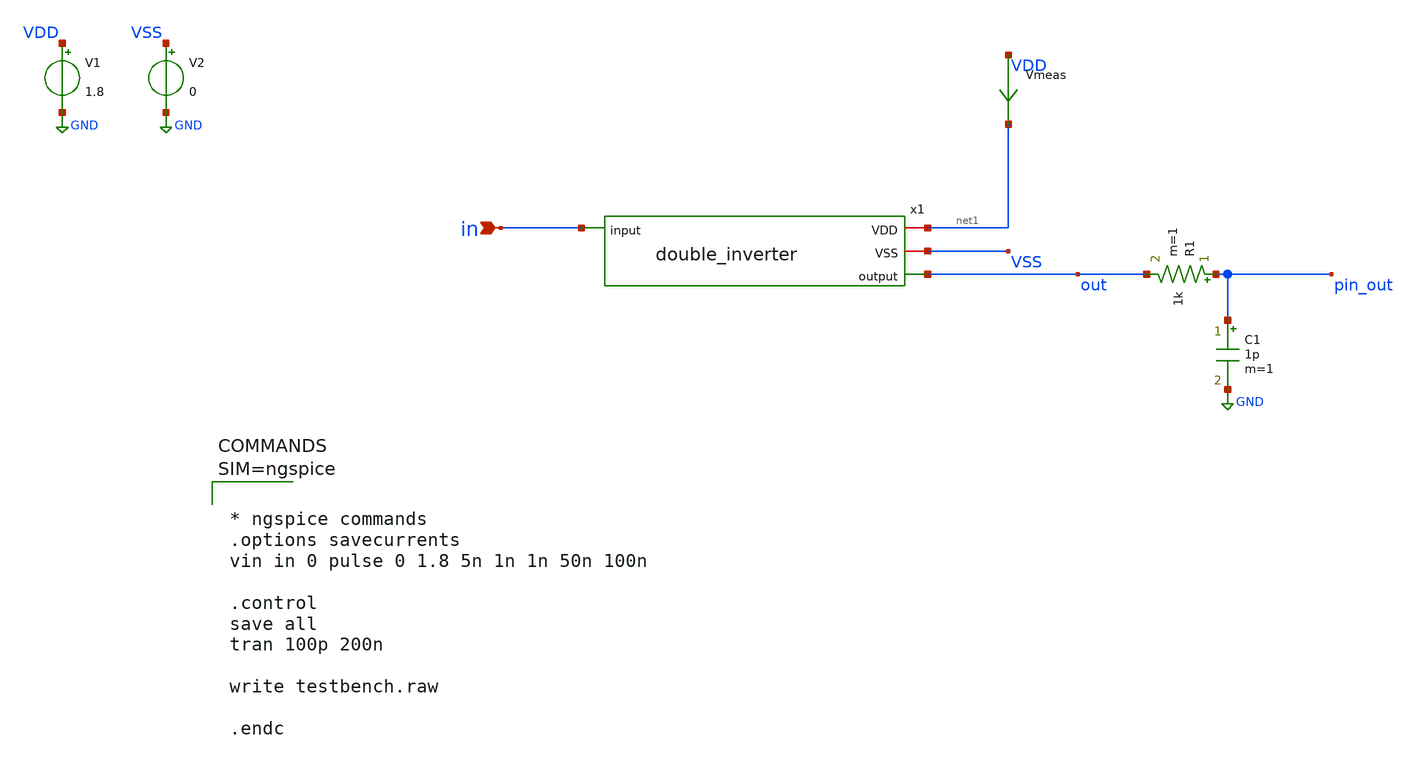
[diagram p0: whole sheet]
** sch_path: xschem/testbench.sch
**.subckt testbench in
*.ipin in
x1 net1 VSS out in double_inverter
V1 VDD GND 1.8
V2 VSS GND 0
R1 pin_out out 1k m=1
C1 pin_out GND 1p m=1
Vmeas VDD net1 0
.save i(vmeas)
**** begin user architecture code

** opencircuitdesign pdks install
.lib $::SKYWATER_MODELS/sky130.lib.spice tt





* ngspice commands
.options savecurrents
vin in 0 pulse 0 1.8 5n 1n 1n 50n 100n

.control
save all
tran 100p 200n

write testbench.raw

.endc



**** end user architecture code
**.ends

* expanding   symbol:  double_inverter.sym # of pins=4
** sym_path: xschem/double_inverter.sym
** sch_path: xschem/double_inverter.sch
.subckt double_inverter VDD VSS output input
*.iopin VDD
*.iopin VSS
*.ipin input
*.opin output
XM1 inverted input VDD VDD sky130_fd_pr__pfet_01v8 L=0.15 W=1 nf=1 ad='int((nf+1)/2) * W/nf * 0.29' as='int((nf+2)/2) * W/nf * 0.29'
+ pd='2*int((nf+1)/2) * (W/nf + 0.29)' ps='2*int((nf+2)/2) * (W/nf + 0.29)' nrd='0.29 / W' nrs='0.29 / W'
+ sa=0 sb=0 sd=0 mult=1 m=1
XM2 inverted input VSS VSS sky130_fd_pr__nfet_01v8 L=0.15 W=1 nf=1 ad='int((nf+1)/2) * W/nf * 0.29' as='int((nf+2)/2) * W/nf * 0.29'
+ pd='2*int((nf+1)/2) * (W/nf + 0.29)' ps='2*int((nf+2)/2) * (W/nf + 0.29)' nrd='0.29 / W' nrs='0.29 / W'
+ sa=0 sb=0 sd=0 mult=1 m=1
XM3 output inverted VDD VDD sky130_fd_pr__pfet_01v8 L=0.15 W=20 nf=20 ad='int((nf+1)/2) * W/nf * 0.29'
+ as='int((nf+2)/2) * W/nf * 0.29' pd='2*int((nf+1)/2) * (W/nf + 0.29)' ps='2*int((nf+2)/2) * (W/nf + 0.29)'
+ nrd='0.29 / W' nrs='0.29 / W' sa=0 sb=0 sd=0 mult=1 m=1
XM4 output inverted VSS VSS sky130_fd_pr__nfet_01v8 L=0.15 W=20 nf=20 ad='int((nf+1)/2) * W/nf * 0.29'
+ as='int((nf+2)/2) * W/nf * 0.29' pd='2*int((nf+1)/2) * (W/nf + 0.29)' ps='2*int((nf+2)/2) * (W/nf + 0.29)'
+ nrd='0.29 / W' nrs='0.29 / W' sa=0 sb=0 sd=0 mult=1 m=1
.ends

.GLOBAL GND
.end
